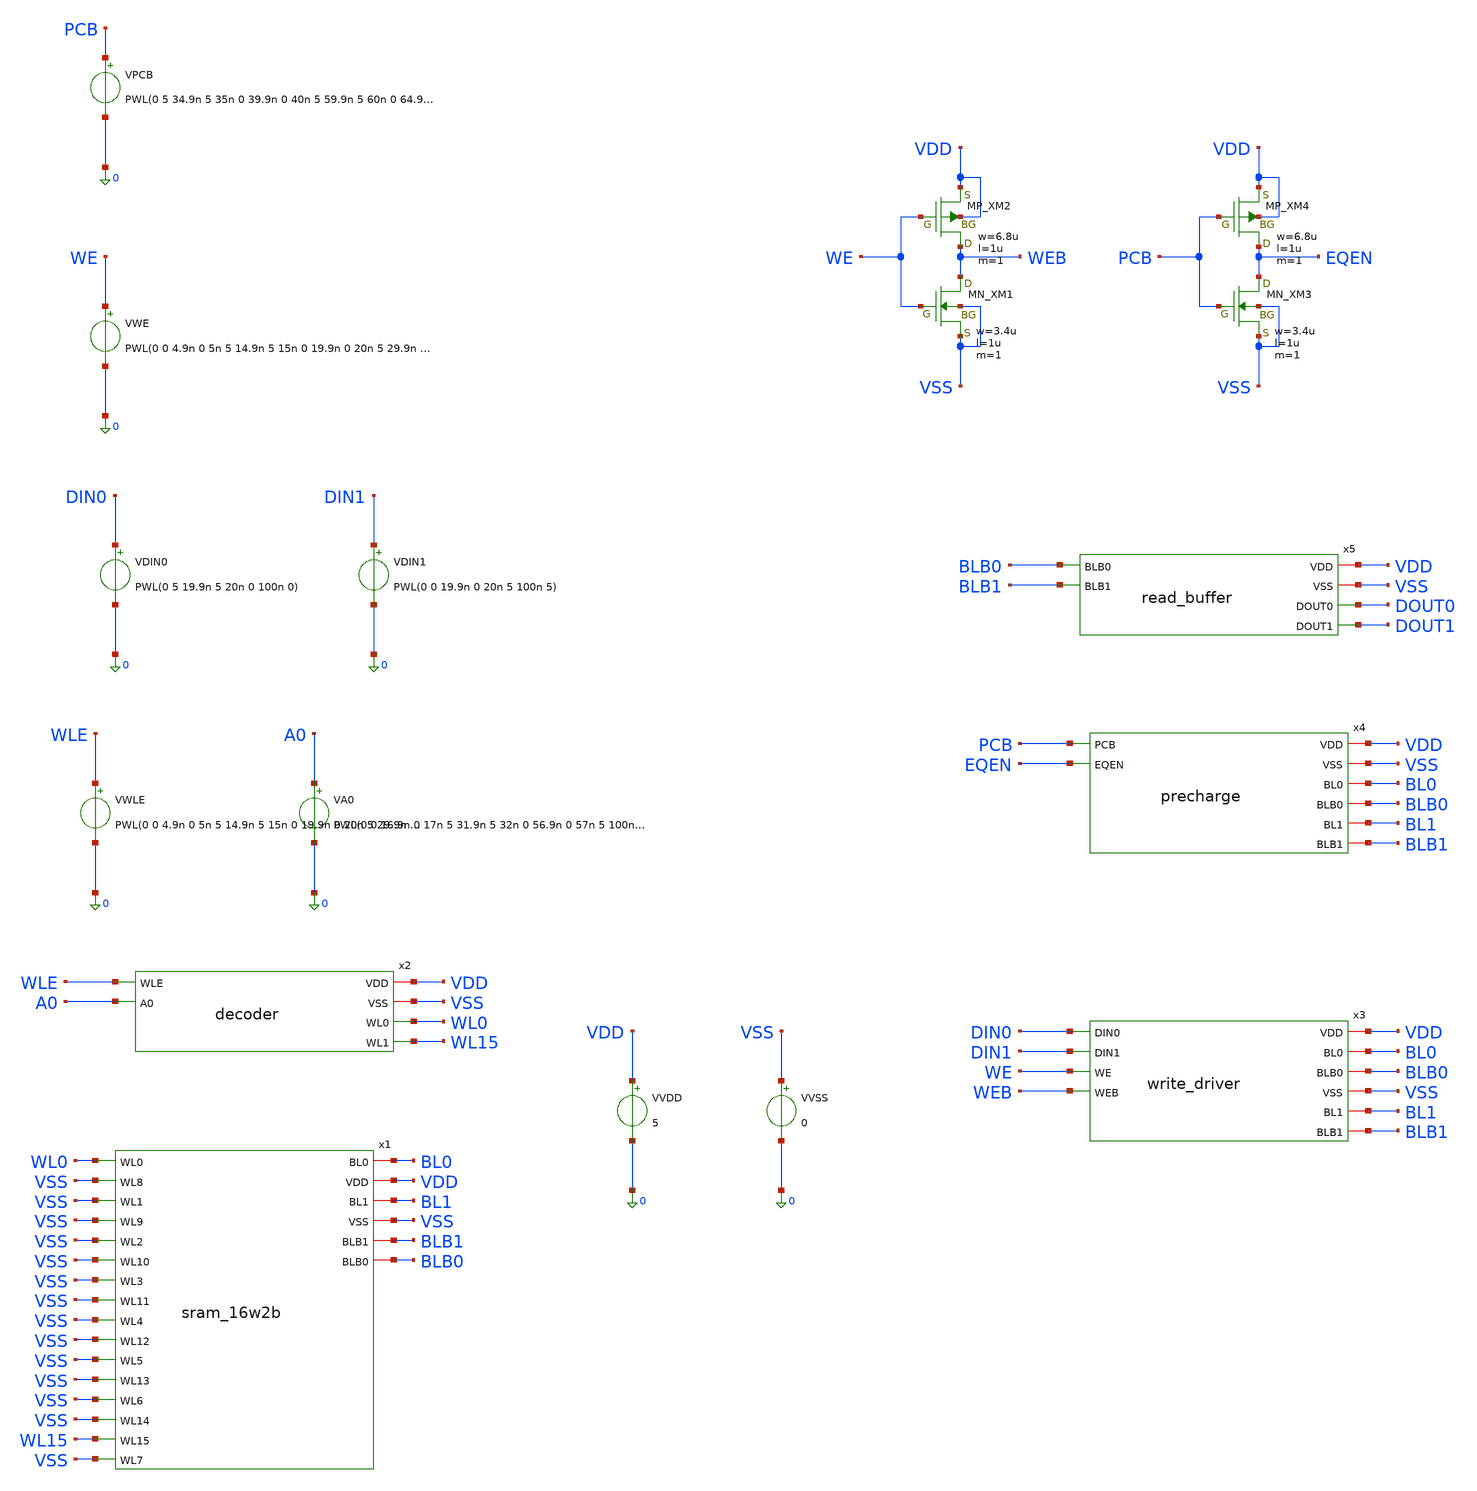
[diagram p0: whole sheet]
** sch_path: sram/tb_sram_16w2b.sch
**.subckt tb_sram_16w2b
VVDD VDD 0 5
VDIN0 DIN0 0 PWL(0 5 19.9n 5 20n 0 100n 0)
VVSS VSS 0 0
VWE WE 0 PWL(0 0 4.9n 0 5n 5 14.9n 5 15n 0 19.9n 0 20n 5 29.9n 5 30n 0 100n 0)
VPCB PCB 0 PWL(0 5 34.9n 5 35n 0 39.9n 0 40n 5 59.9n 5 60n 0 64.9n 0 65n 5 100n 5)
x2 VDD VSS WL0 WLE A0 WL15 decoder
VWLE WLE 0 PWL(0 0 4.9n 0 5n 5 14.9n 5 15n 0 19.9n 0 20n 5 29.9n 5 30n 0 44.9n 0 45n 5 54.9n 5 55n 0
+ 69.9n 0 70n 5 79.9n 5 80n 0 100n 0)
VA0 A0 0 PWL(0 0 16.9n 0 17n 5 31.9n 5 32n 0 56.9n 0 57n 5 100n 5)
x3 DIN0 VDD BL0 BLB0 VSS DIN1 BL1 WE BLB1 WEB write_driver
VDIN1 DIN1 0 PWL(0 0 19.9n 0 20n 5 100n 5)
x4 VDD VSS PCB EQEN BL0 BLB0 BL1 BLB1 precharge
x5 VDD VSS BLB0 BLB1 DOUT0 DOUT1 read_buffer
XXM1 WEB WE VSS VSS NMOS w=3.4u l=1u nrd=0 nrs=0 m=1
XXM2 WEB WE VDD VDD PMOS w=6.8u l=1u nrd=0 nrs=0 m=1
XXM3 EQEN PCB VSS VSS NMOS w=3.4u l=1u nrd=0 nrs=0 m=1
XXM4 EQEN PCB VDD VDD PMOS w=6.8u l=1u nrd=0 nrs=0 m=1
x1 BL0 VDD WL0 VSS BL1 VSS VSS BLB1 VSS BLB0 VSS VSS VSS VSS VSS VSS VSS VSS VSS VSS WL15 VSS
+ sram_16w2b
**** begin user architecture code
 .include $::LIB/ip62_models



.tran 10p 100n

* ============================================================
* RowMax 16w2b SRAM Read Measurement
* Active rows: WL0 and WL15
* Observe: bit0 and bit1
* ============================================================

* Read access time
.meas tran t_read0 TRIG v(WL0)  VAL=2.5 RISE=2
                    TARG v(DOUT0) VAL=2.5 RISE=1 TD=40n

.meas tran t_read15 TRIG v(WL15) VAL=2.5 RISE=2
                     TARG v(DOUT1) VAL=2.5 RISE=1 TD=65n

* WL0 read timing
.meas tran t_wl0_rise WHEN v(WL0)=2.5 RISE=2
.meas tran t_dout0_rise WHEN v(DOUT0)=2.5 RISE=1 TD=40n
.meas tran td_read0 PARAM='t_dout0_rise-t_wl0_rise'

* Bit-line differential
.meas tran dvbl0_05 FIND par('abs(v(BL0)-v(BLB0))') AT=46.88n
.meas tran dvbl0_10 FIND par('abs(v(BL0)-v(BLB0))') AT=47.38n

.meas tran dvbl1_05 FIND par('abs(v(BL1)-v(BLB1))') AT=46.88n
.meas tran dvbl1_10 FIND par('abs(v(BL1)-v(BLB1))') AT=47.38n

.control
run

plot v(pcb) v(eqen)+6
plot v(wl0) v(wl15)+6
plot v(dout0)+12 v(dout1)+18
plot v(bl0) v(blb0)
plot v(bl1) v(blb1)

.endc


**** end user architecture code
**.ends
.end
